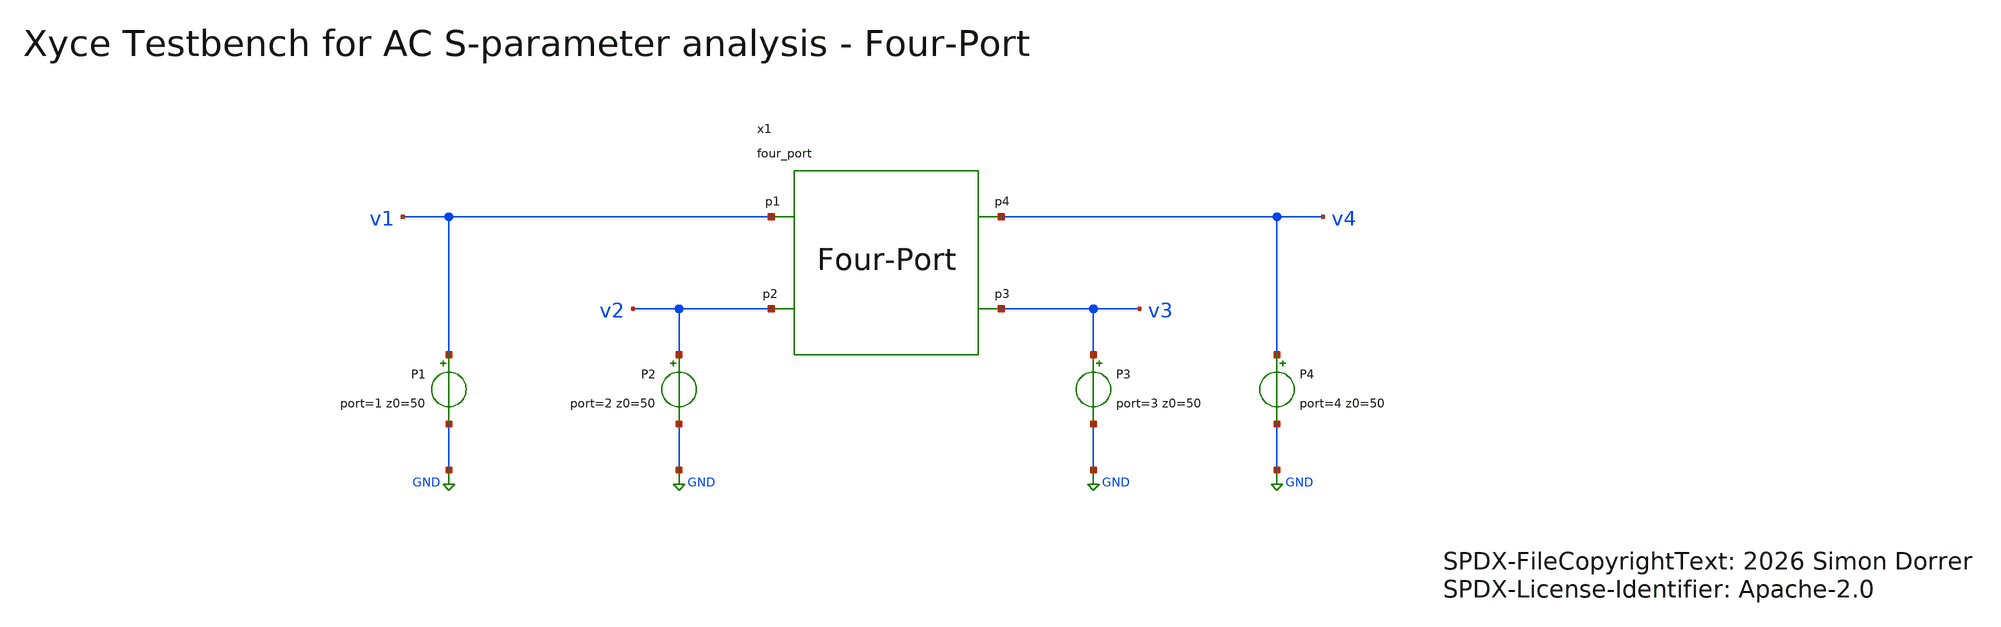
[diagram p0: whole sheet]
** sch_path: testbenches/xschem/four_port_tb_acsp_xyce.sch
* SPDX-FileCopyrightText: 2026 Simon Dorrer
* SPDX-License-Identifier: Apache-2.0
**.subckt four_port_tb_acsp_xyce
P2 v2 GND port=2 z0=50
P3 v3 GND port=3 z0=50
P4 v4 GND port=4 z0=50
x1 v1 v2 v3 v4 four_port
P1 v1 GND port=1 z0=50
**** begin user architecture code


.include ../../../netlist/xyce/four_port.cir
.include ../sim_range.cir

* User Constants
* f_min / f_max come from ../sim_range.cir (.param),
* auto-synced by snp2le to the band it fitted.
* edit that file for a standalone run.

* Xschem's ground symbol netlists node GND, which Xyce takes as ground only with this.
.PREPROCESS REPLACEGROUND TRUE

* AC S-Parameter Analysis
* Xyce writes S-parameters only as a Touchstone file, which snp2le imports.
.AC LIN 1001 {f_min} {f_max}
.LIN SPARCALC=1 FORMAT=TOUCHSTONE2 DATAFORMAT=RI FILE=../plot_simulations/data/@schname\.s4p


**** end user architecture code
**.ends
.GLOBAL GND
.end
